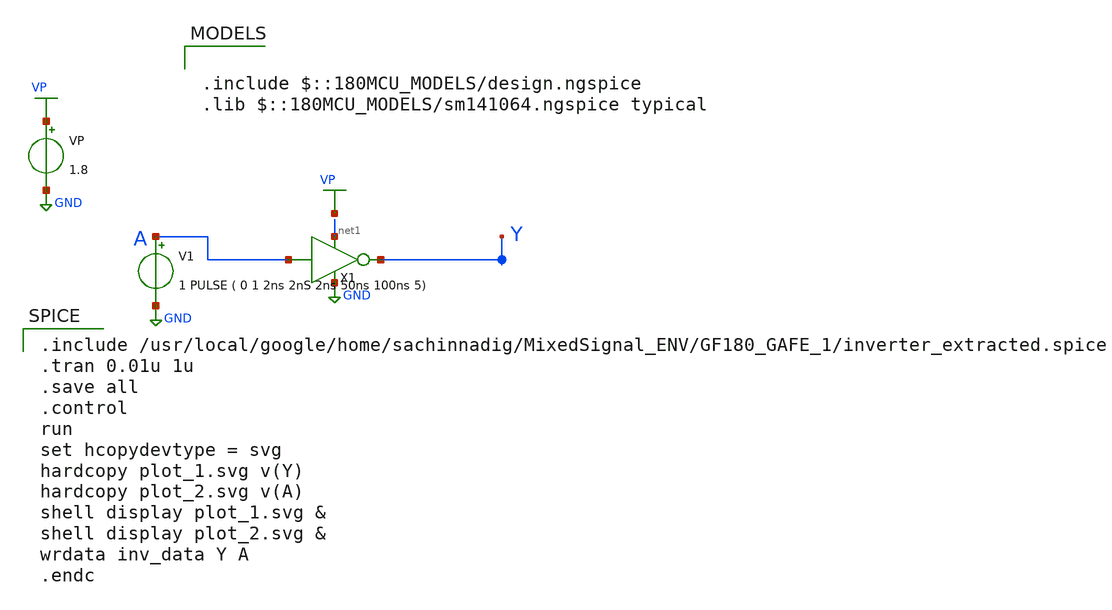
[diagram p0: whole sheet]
** sch_path: inverter_extracted.sch
**.subckt inverter_extracted
VP VP GND 1.8
X1 net1 GND Y A inverter_extracted
V1 A GND 1 PULSE ( 0 1 2ns 2nS 2ns 50ns 100ns 5)
**** begin user architecture code

.include $::180MCU_MODELS/design.ngspice
.lib $::180MCU_MODELS/sm141064.ngspice typical


.include /usr/local/google/home/sachinnadig/MixedSignal_ENV/GF180_GAFE_1/inverter_extracted.spice
.tran 0.01u 1u
.save all
.control
run
set hcopydevtype = svg
hardcopy plot_1.svg v(Y)
hardcopy plot_2.svg v(A)
shell display plot_1.svg &
shell display plot_2.svg &
wrdata inv_data Y A
.endc

**** end user architecture code
**.ends
.GLOBAL VP
.GLOBAL GND
.end
